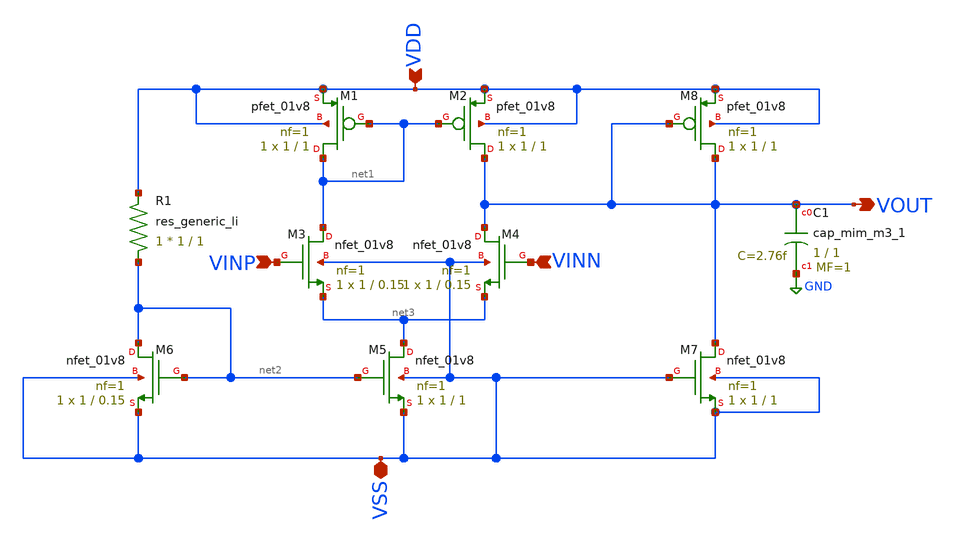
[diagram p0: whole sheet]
** sch_path: schematics/bootcamp_opamp.sch
**.subckt bootcamp_opamp VSS VOUT VDD VINP VINN
*.iopin VSS
*.opin VOUT
*.ipin VDD
*.ipin VINP
*.ipin VINN
XM1 net1 net1 VDD VDD sky130_fd_pr__pfet_01v8 L=1 W=1 nf=1 ad='int((nf+1)/2) * W/nf * 0.29' as='int((nf+2)/2) * W/nf * 0.29'
+ pd='2*int((nf+1)/2) * (W/nf + 0.29)' ps='2*int((nf+2)/2) * (W/nf + 0.29)' nrd='0.29 / W' nrs='0.29 / W'
+ sa=0 sb=0 sd=0 mult=1 m=1
XM2 VOUT net1 VDD VDD sky130_fd_pr__pfet_01v8 L=1 W=1 nf=1 ad='int((nf+1)/2) * W/nf * 0.29' as='int((nf+2)/2) * W/nf * 0.29'
+ pd='2*int((nf+1)/2) * (W/nf + 0.29)' ps='2*int((nf+2)/2) * (W/nf + 0.29)' nrd='0.29 / W' nrs='0.29 / W'
+ sa=0 sb=0 sd=0 mult=1 m=1
XM3 net1 VINP net3 VSS sky130_fd_pr__nfet_01v8 L=0.15 W=1 nf=1 ad='int((nf+1)/2) * W/nf * 0.29' as='int((nf+2)/2) * W/nf * 0.29'
+ pd='2*int((nf+1)/2) * (W/nf + 0.29)' ps='2*int((nf+2)/2) * (W/nf + 0.29)' nrd='0.29 / W' nrs='0.29 / W'
+ sa=0 sb=0 sd=0 mult=1 m=1
XM4 VOUT VINN net3 VSS sky130_fd_pr__nfet_01v8 L=0.15 W=1 nf=1 ad='int((nf+1)/2) * W/nf * 0.29' as='int((nf+2)/2) * W/nf * 0.29'
+ pd='2*int((nf+1)/2) * (W/nf + 0.29)' ps='2*int((nf+2)/2) * (W/nf + 0.29)' nrd='0.29 / W' nrs='0.29 / W'
+ sa=0 sb=0 sd=0 mult=1 m=1
XM5 net3 net2 VSS VSS sky130_fd_pr__nfet_01v8 L=1 W=1 nf=1 ad='int((nf+1)/2) * W/nf * 0.29' as='int((nf+2)/2) * W/nf * 0.29'
+ pd='2*int((nf+1)/2) * (W/nf + 0.29)' ps='2*int((nf+2)/2) * (W/nf + 0.29)' nrd='0.29 / W' nrs='0.29 / W'
+ sa=0 sb=0 sd=0 mult=1 m=1
XM6 net2 net2 VSS VSS sky130_fd_pr__nfet_01v8 L=0.15 W=1 nf=1 ad='int((nf+1)/2) * W/nf * 0.29' as='int((nf+2)/2) * W/nf * 0.29'
+ pd='2*int((nf+1)/2) * (W/nf + 0.29)' ps='2*int((nf+2)/2) * (W/nf + 0.29)' nrd='0.29 / W' nrs='0.29 / W'
+ sa=0 sb=0 sd=0 mult=1 m=1
XM7 VOUT VSS VSS VSS sky130_fd_pr__nfet_01v8 L=1 W=1 nf=1 ad='int((nf+1)/2) * W/nf * 0.29' as='int((nf+2)/2) * W/nf * 0.29'
+ pd='2*int((nf+1)/2) * (W/nf + 0.29)' ps='2*int((nf+2)/2) * (W/nf + 0.29)' nrd='0.29 / W' nrs='0.29 / W'
+ sa=0 sb=0 sd=0 mult=1 m=1
XM8 VOUT VOUT VDD VDD sky130_fd_pr__pfet_01v8 L=1 W=1 nf=1 ad='int((nf+1)/2) * W/nf * 0.29' as='int((nf+2)/2) * W/nf * 0.29'
+ pd='2*int((nf+1)/2) * (W/nf + 0.29)' ps='2*int((nf+2)/2) * (W/nf + 0.29)' nrd='0.29 / W' nrs='0.29 / W'
+ sa=0 sb=0 sd=0 mult=1 m=1
R1 net2 VDD sky130_fd_pr__res_generic_li W=1 L=1 m=1
XC1 VOUT GND sky130_fd_pr__cap_mim_m3_1 W=1 L=1 MF=1 m=1
**.ends
.GLOBAL GND
.end
